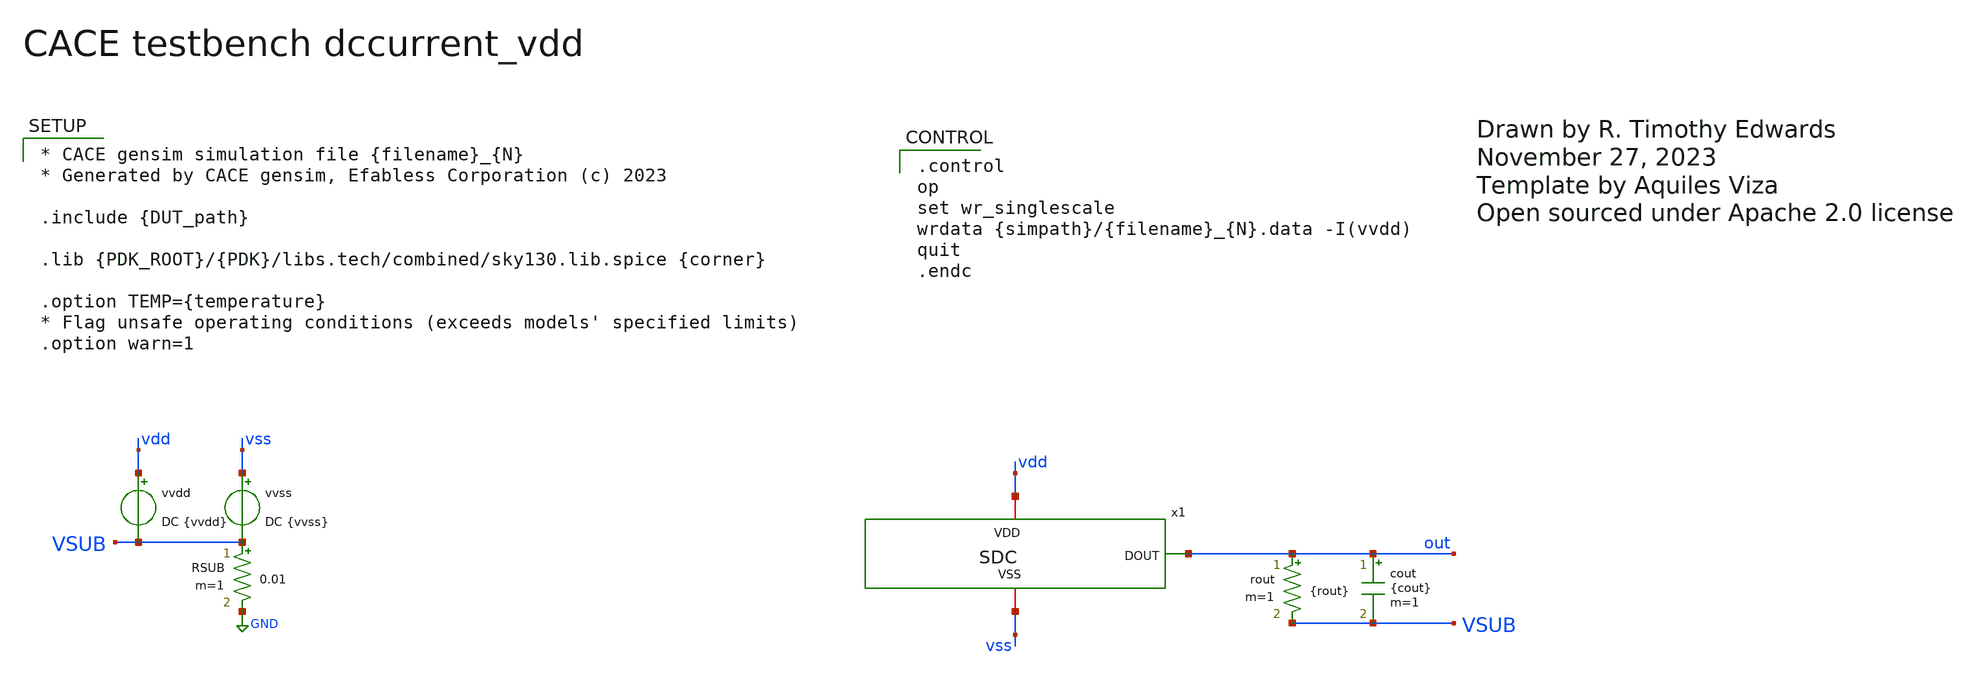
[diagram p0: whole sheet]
** sch_path: samples/cace-tests/SDC/cace/dccurrent_vdd.sch
* Open sourced under Apache 2.0 license

* CACE gensim simulation file {filename}_{N}
* Generated by CACE gensim, Efabless Corporation (c) 2023

.include {DUT_path}

.lib {PDK_ROOT}/{PDK}/libs.tech/combined/sky130.lib.spice {corner}

.option TEMP={temperature}
* Flag unsafe operating conditions (exceeds models' specified limits)
.option warn=1


**.subckt dccurrent_vdd
vvss vss VSUB DC {vvss}
rout out VSUB {rout} m=1
cout out VSUB {cout} m=1
vvdd vdd VSUB DC {vvdd}
RSUB VSUB GND 0.01 m=1
x1 vdd out vss SDC
**** begin user architecture code

.control
op
set wr_singlescale
wrdata {simpath}/{filename}_{N}.data -I(vvdd)
quit
.endc


**** end user architecture code
**.ends
.GLOBAL GND
.end
